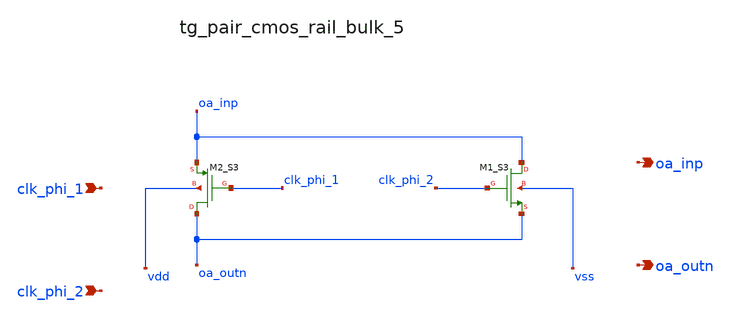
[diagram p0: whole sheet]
** sch_path: analog-db/raw/sup_003_rrl_sc_integrator/hier/blocks/tg_pair_cmos_rail_bulk_5.sch
**.subckt tg_pair_cmos_rail_bulk_5 clk_phi_1 clk_phi_2 oa_inp oa_outn
*.ipin clk_phi_1
*.ipin clk_phi_2
*.opin oa_inp
*.opin oa_outn
XM1_S3 oa_inp clk_phi_2 oa_outn vss sg13_lv_nmos w=x_dut_xm1_s3_w l=x_dut_xm1_s3_l ng=1
+ m=x_dut_xm1_s3_m
XM2_S3 oa_outn clk_phi_1 oa_inp vdd sg13_lv_pmos w=x_dut_xm2_s3_w l=x_dut_xm2_s3_l ng=1
+ m=x_dut_xm2_s3_m
**.ends
.end
